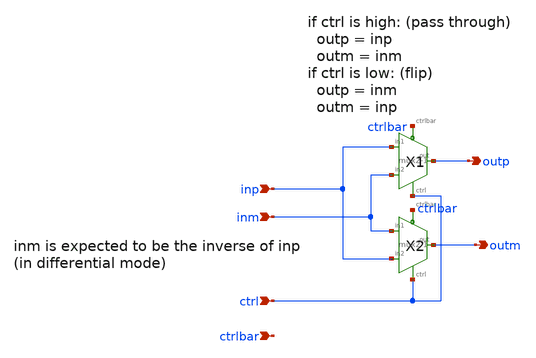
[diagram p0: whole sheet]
** sch_path: xschem/mux/multiplier_differential.sch
**.subckt multiplier_differential inp inm outp outm ctrl ctrlbar
*.ipin inp
*.ipin inm
*.opin outp
*.opin outm
*.ipin ctrl
*.ipin ctrlbar
X1 inp outp inm ctrl ctrlbar mux2-1
X2 inm outm inp ctrl ctrlbar mux2-1
**.ends
.end
